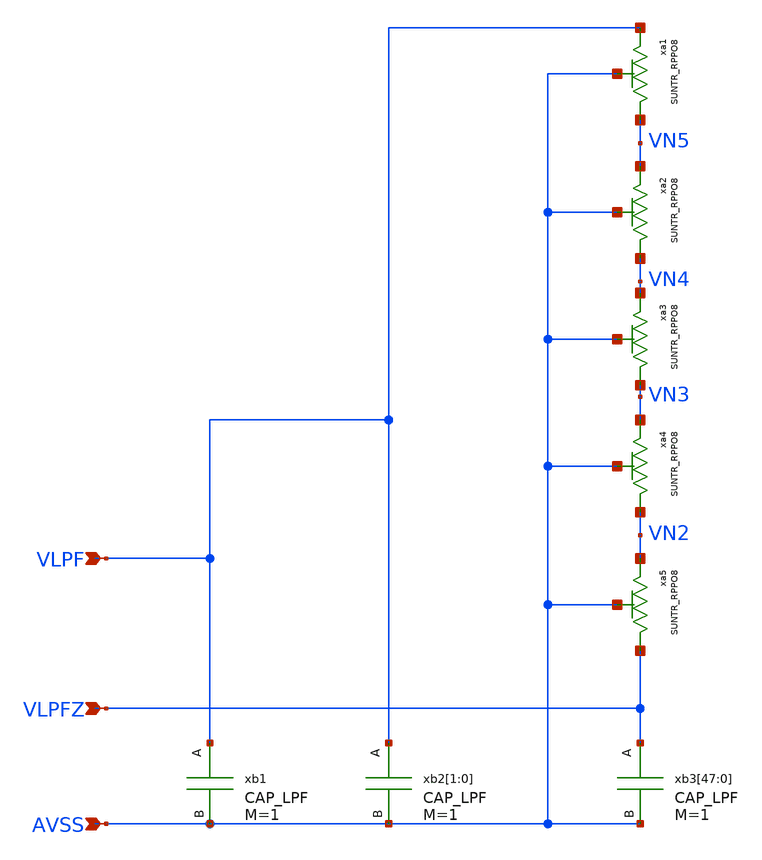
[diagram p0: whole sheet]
** sch_path: design/SUN_PLL_SKY130NM/SUN_PLL_LPF.sch
**.subckt SUN_PLL_LPF VLPF AVSS VLPFZ
*.ipin VLPF
*.ipin AVSS
*.ipin VLPFZ
xa5 VLPFZ VN2 AVSS SUNTR_RPPO8 xoffset=0 yoffset=2 angle=0 M=1
xb3[47] VLPFZ AVSS CAP_LPF xoffset=0 yoffset=0 angle=0 M=1
xb3[46] VLPFZ AVSS CAP_LPF xoffset=0 yoffset=0 angle=0 M=1
xb3[45] VLPFZ AVSS CAP_LPF xoffset=0 yoffset=0 angle=0 M=1
xb3[44] VLPFZ AVSS CAP_LPF xoffset=0 yoffset=0 angle=0 M=1
xb3[43] VLPFZ AVSS CAP_LPF xoffset=0 yoffset=0 angle=0 M=1
xb3[42] VLPFZ AVSS CAP_LPF xoffset=0 yoffset=0 angle=0 M=1
xb3[41] VLPFZ AVSS CAP_LPF xoffset=0 yoffset=0 angle=0 M=1
xb3[40] VLPFZ AVSS CAP_LPF xoffset=0 yoffset=0 angle=0 M=1
xb3[39] VLPFZ AVSS CAP_LPF xoffset=0 yoffset=0 angle=0 M=1
xb3[38] VLPFZ AVSS CAP_LPF xoffset=0 yoffset=0 angle=0 M=1
xb3[37] VLPFZ AVSS CAP_LPF xoffset=0 yoffset=0 angle=0 M=1
xb3[36] VLPFZ AVSS CAP_LPF xoffset=0 yoffset=0 angle=0 M=1
xb3[35] VLPFZ AVSS CAP_LPF xoffset=0 yoffset=0 angle=0 M=1
xb3[34] VLPFZ AVSS CAP_LPF xoffset=0 yoffset=0 angle=0 M=1
xb3[33] VLPFZ AVSS CAP_LPF xoffset=0 yoffset=0 angle=0 M=1
xb3[32] VLPFZ AVSS CAP_LPF xoffset=0 yoffset=0 angle=0 M=1
xb3[31] VLPFZ AVSS CAP_LPF xoffset=0 yoffset=0 angle=0 M=1
xb3[30] VLPFZ AVSS CAP_LPF xoffset=0 yoffset=0 angle=0 M=1
xb3[29] VLPFZ AVSS CAP_LPF xoffset=0 yoffset=0 angle=0 M=1
xb3[28] VLPFZ AVSS CAP_LPF xoffset=0 yoffset=0 angle=0 M=1
xb3[27] VLPFZ AVSS CAP_LPF xoffset=0 yoffset=0 angle=0 M=1
xb3[26] VLPFZ AVSS CAP_LPF xoffset=0 yoffset=0 angle=0 M=1
xb3[25] VLPFZ AVSS CAP_LPF xoffset=0 yoffset=0 angle=0 M=1
xb3[24] VLPFZ AVSS CAP_LPF xoffset=0 yoffset=0 angle=0 M=1
xb3[23] VLPFZ AVSS CAP_LPF xoffset=0 yoffset=0 angle=0 M=1
xb3[22] VLPFZ AVSS CAP_LPF xoffset=0 yoffset=0 angle=0 M=1
xb3[21] VLPFZ AVSS CAP_LPF xoffset=0 yoffset=0 angle=0 M=1
xb3[20] VLPFZ AVSS CAP_LPF xoffset=0 yoffset=0 angle=0 M=1
xb3[19] VLPFZ AVSS CAP_LPF xoffset=0 yoffset=0 angle=0 M=1
xb3[18] VLPFZ AVSS CAP_LPF xoffset=0 yoffset=0 angle=0 M=1
xb3[17] VLPFZ AVSS CAP_LPF xoffset=0 yoffset=0 angle=0 M=1
xb3[16] VLPFZ AVSS CAP_LPF xoffset=0 yoffset=0 angle=0 M=1
xb3[15] VLPFZ AVSS CAP_LPF xoffset=0 yoffset=0 angle=0 M=1
xb3[14] VLPFZ AVSS CAP_LPF xoffset=0 yoffset=0 angle=0 M=1
xb3[13] VLPFZ AVSS CAP_LPF xoffset=0 yoffset=0 angle=0 M=1
xb3[12] VLPFZ AVSS CAP_LPF xoffset=0 yoffset=0 angle=0 M=1
xb3[11] VLPFZ AVSS CAP_LPF xoffset=0 yoffset=0 angle=0 M=1
xb3[10] VLPFZ AVSS CAP_LPF xoffset=0 yoffset=0 angle=0 M=1
xb3[9] VLPFZ AVSS CAP_LPF xoffset=0 yoffset=0 angle=0 M=1
xb3[8] VLPFZ AVSS CAP_LPF xoffset=0 yoffset=0 angle=0 M=1
xb3[7] VLPFZ AVSS CAP_LPF xoffset=0 yoffset=0 angle=0 M=1
xb3[6] VLPFZ AVSS CAP_LPF xoffset=0 yoffset=0 angle=0 M=1
xb3[5] VLPFZ AVSS CAP_LPF xoffset=0 yoffset=0 angle=0 M=1
xb3[4] VLPFZ AVSS CAP_LPF xoffset=0 yoffset=0 angle=0 M=1
xb3[3] VLPFZ AVSS CAP_LPF xoffset=0 yoffset=0 angle=0 M=1
xb3[2] VLPFZ AVSS CAP_LPF xoffset=0 yoffset=0 angle=0 M=1
xb3[1] VLPFZ AVSS CAP_LPF xoffset=0 yoffset=0 angle=0 M=1
xb3[0] VLPFZ AVSS CAP_LPF xoffset=0 yoffset=0 angle=0 M=1
xb2[1] VLPF AVSS CAP_LPF xoffset=0 yoffset=0 angle=0 M=1
xb2[0] VLPF AVSS CAP_LPF xoffset=0 yoffset=0 angle=0 M=1
xb1 VLPF AVSS CAP_LPF xoffset=0 yoffset=0 angle=0 M=1
xa4 VN2 VN3 AVSS SUNTR_RPPO8 xoffset=0 yoffset=2 angle=0 M=1
xa3 VN3 VN4 AVSS SUNTR_RPPO8 xoffset=0 yoffset=2 angle=0 M=1
xa2 VN4 VN5 AVSS SUNTR_RPPO8 xoffset=0 yoffset=2 angle=0 M=1
xa1 VN5 VLPF AVSS SUNTR_RPPO8 xoffset=0 yoffset=2 angle=0 M=1
**.ends

* expanding   symbol:  SUN_TR_SKY130NM/SUNTR_RPPO8.sym # of pins=3
** sym_path: SUN_TR_SKY130NM/SUNTR_RPPO8.sym
** sch_path: SUN_TR_SKY130NM/SUNTR_RPPO8.sch
.subckt SUNTR_RPPO8 N P B  xoffset=0 yoffset=0 angle=0 M=1
*.iopin P
*.iopin N
*.iopin B
XXA1 N P B SUNTR_RES8 xoffset=0 yoffset=0 angle=0
.ends


* expanding   symbol:  SUN_PLL_SKY130NM/CAP_LPF.sym # of pins=2
** sym_path: SUN_PLL_SKY130NM/CAP_LPF.sym
** sch_path: SUN_PLL_SKY130NM/CAP_LPF.sch
.subckt CAP_LPF A B  xoffset=0 yoffset=0 angle=0 M=1
*.iopin A
*.iopin B
R1 A NC0 sky130_fd_pr__res_generic_m1 W=0.4 L=0.4 m=1
R2 B NC1 sky130_fd_pr__res_generic_m1 W=0.4 L=0.4 m=1
.ends


* expanding   symbol:  SUN_TR_SKY130NM/SUNTR_RES8.sym # of pins=3
** sym_path: SUN_TR_SKY130NM/SUNTR_RES8.sym
** sch_path: SUN_TR_SKY130NM/SUNTR_RES8.sch
.subckt SUNTR_RES8 N P B  xoffset=0 yoffset=0 angle=0
*.iopin N
*.iopin P
*.iopin B
XR1_0 INT_0 N B sky130_fd_pr__res_high_po W=0.72 L=8.8 mult=1 m=1
XR1_1 INT_1 INT_0 B sky130_fd_pr__res_high_po W=0.72 L=8.8 mult=1 m=1
XR1_2 INT_2 INT_1 B sky130_fd_pr__res_high_po W=0.72 L=8.8 mult=1 m=1
XR1_3 INT_3 INT_2 B sky130_fd_pr__res_high_po W=0.72 L=8.8 mult=1 m=1
XR1_4 INT_4 INT_3 B sky130_fd_pr__res_high_po W=0.72 L=8.8 mult=1 m=1
XR1_5 INT_5 INT_4 B sky130_fd_pr__res_high_po W=0.72 L=8.8 mult=1 m=1
XR1_6 INT_6 INT_5 B sky130_fd_pr__res_high_po W=0.72 L=8.8 mult=1 m=1
XR1_7 P INT_6 B sky130_fd_pr__res_high_po W=0.72 L=8.8 mult=1 m=1
.ends

.end
